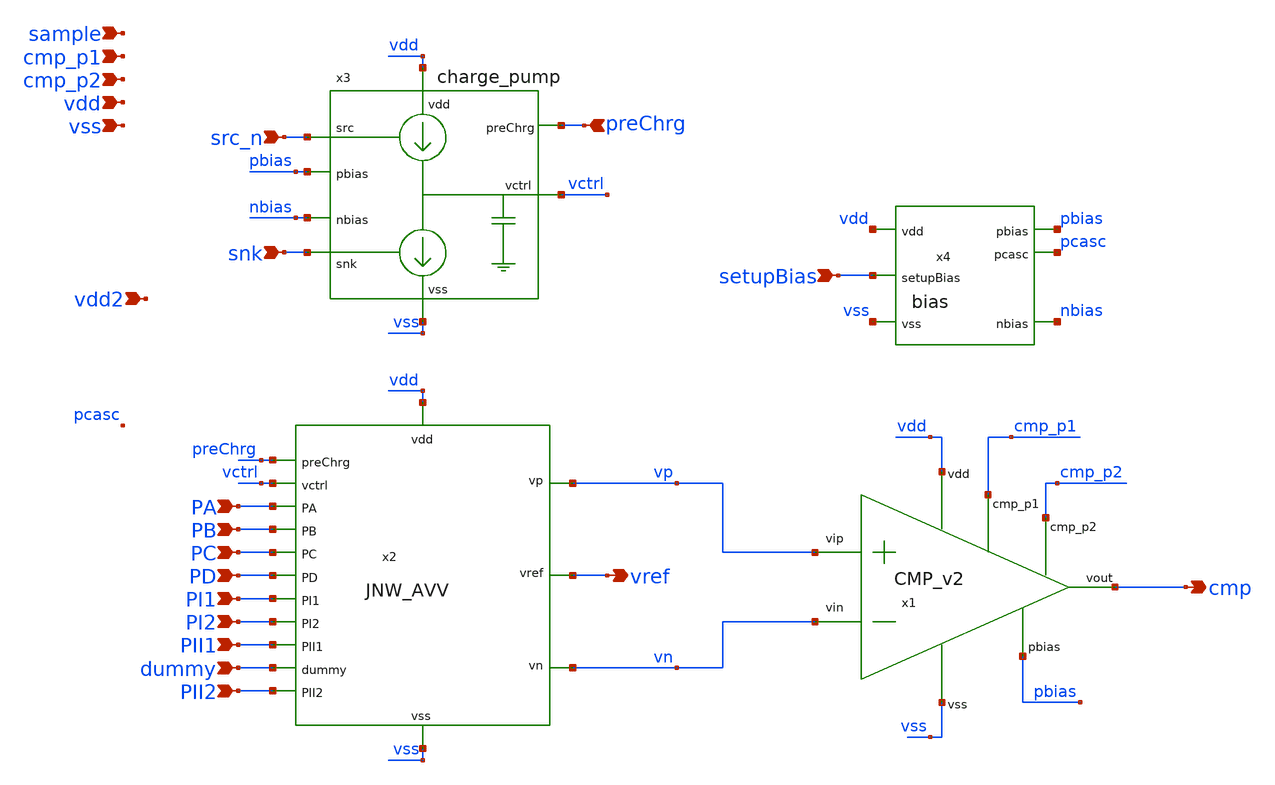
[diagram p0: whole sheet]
** sch_path: design/JNW_AVV_SKY130A/TB_bandgap.sch
**.subckt TB_bandgap vdd2 vss vref src_n snk PA PB PC PD PI1 PI2 PII1 cmp preChrg dummy PII2
*+ setupBias cmp_p1 cmp_p2 sample vdd
*.ipin vdd2
*.ipin vss
*.opin vref
*.ipin src_n
*.ipin snk
*.ipin PA
*.ipin PB
*.ipin PC
*.ipin PD
*.ipin PI1
*.ipin PI2
*.ipin PII1
*.opin cmp
*.ipin preChrg
*.ipin dummy
*.ipin PII2
*.ipin setupBias
*.ipin cmp_p1
*.ipin cmp_p2
*.ipin sample
*.ipin vdd
x3 vdd pbias src_n vctrl snk nbias vss preChrg charge_pump
x2 vctrl PA PD vref vdd vss PC PB dummy PI2 PI1 PII1 vn vp PII2 preChrg JNW_AVV
x4 pbias vdd nbias vss setupBias pcasc bias
x1 vdd pbias cmp vn vp vss cmp_p1 cmp_p2 CMP_v2
**.ends
.end
